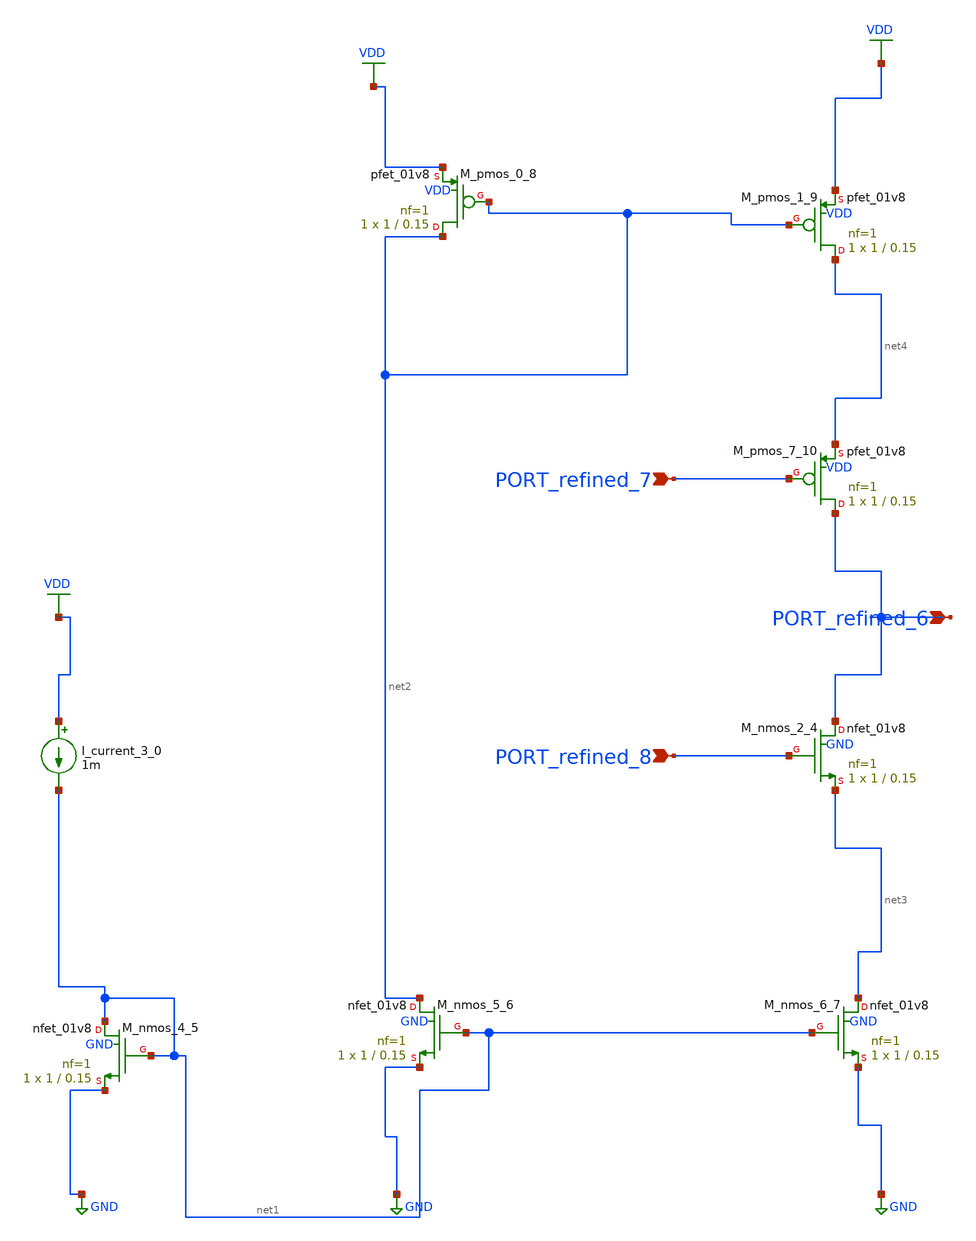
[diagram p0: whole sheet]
** sch_path: schematics/SchemGen/10_1007_s10470-024-02258-z_05_001.sch
**.subckt 10_1007_s10470-024-02258-z_05_001 PORT_refined_6 PORT_refined_7 PORT_refined_8
*.ipin PORT_refined_6
*.ipin PORT_refined_7
*.ipin PORT_refined_8
I_current_3_0 VDD net1 1m
XM_nmos_2_4 PORT_refined_6 PORT_refined_8 net3 GND sky130_fd_pr__nfet_01v8 L=0.15 W=1 nf=1 ad='int((1 + 1)/2) * 1 / 1 * 0.29'
+ as='int((1 + 2)/2) * 1 / 1 * 0.29' pd='2*int((1 + 1)/2) * (1 / 1 + 0.29)' ps='2*int((1 + 2)/2) * (1 / 1 + 0.29)'
+ nrd='0.29 / 1 ' nrs='0.29 / 1 ' sa=0 sb=0 sd=0 mult=1 m=1
XM_nmos_4_5 net1 net1 GND GND sky130_fd_pr__nfet_01v8 L=0.15 W=1 nf=1 ad='int((1 + 1)/2) * 1 / 1 * 0.29'
+ as='int((1 + 2)/2) * 1 / 1 * 0.29' pd='2*int((1 + 1)/2) * (1 / 1 + 0.29)' ps='2*int((1 + 2)/2) * (1 / 1 + 0.29)'
+ nrd='0.29 / 1 ' nrs='0.29 / 1 ' sa=0 sb=0 sd=0 mult=1 m=1
XM_nmos_5_6 net2 net1 GND GND sky130_fd_pr__nfet_01v8 L=0.15 W=1 nf=1 ad='int((1 + 1)/2) * 1 / 1 * 0.29'
+ as='int((1 + 2)/2) * 1 / 1 * 0.29' pd='2*int((1 + 1)/2) * (1 / 1 + 0.29)' ps='2*int((1 + 2)/2) * (1 / 1 + 0.29)'
+ nrd='0.29 / 1 ' nrs='0.29 / 1 ' sa=0 sb=0 sd=0 mult=1 m=1
XM_nmos_6_7 net3 net1 GND GND sky130_fd_pr__nfet_01v8 L=0.15 W=1 nf=1 ad='int((1 + 1)/2) * 1 / 1 * 0.29'
+ as='int((1 + 2)/2) * 1 / 1 * 0.29' pd='2*int((1 + 1)/2) * (1 / 1 + 0.29)' ps='2*int((1 + 2)/2) * (1 / 1 + 0.29)'
+ nrd='0.29 / 1 ' nrs='0.29 / 1 ' sa=0 sb=0 sd=0 mult=1 m=1
XM_pmos_0_8 net2 net2 VDD VDD sky130_fd_pr__pfet_01v8 L=0.15 W=1 nf=1 ad='int((1 + 1)/2) * 1 / 1 * 0.29'
+ as='int((1 + 2)/2) * 1 / 1 * 0.29' pd='2*int((1 + 1)/2) * (1 / 1 + 0.29)' ps='2*int((1 + 2)/2) * (1 / 1 + 0.29)'
+ nrd='0.29 / 1 ' nrs='0.29 / 1 ' sa=0 sb=0 sd=0 mult=1 m=1
XM_pmos_1_9 net4 net2 VDD VDD sky130_fd_pr__pfet_01v8 L=0.15 W=1 nf=1 ad='int((1 + 1)/2) * 1 / 1 * 0.29'
+ as='int((1 + 2)/2) * 1 / 1 * 0.29' pd='2*int((1 + 1)/2) * (1 / 1 + 0.29)' ps='2*int((1 + 2)/2) * (1 / 1 + 0.29)'
+ nrd='0.29 / 1 ' nrs='0.29 / 1 ' sa=0 sb=0 sd=0 mult=1 m=1
XM_pmos_7_10 PORT_refined_6 PORT_refined_7 net4 VDD sky130_fd_pr__pfet_01v8 L=0.15 W=1 nf=1 ad='int((1 + 1)/2) * 1 / 1 * 0.29'
+ as='int((1 + 2)/2) * 1 / 1 * 0.29' pd='2*int((1 + 1)/2) * (1 / 1 + 0.29)' ps='2*int((1 + 2)/2) * (1 / 1 + 0.29)'
+ nrd='0.29 / 1 ' nrs='0.29 / 1 ' sa=0 sb=0 sd=0 mult=1 m=1
**.ends
.GLOBAL GND
.GLOBAL VDD
.end
